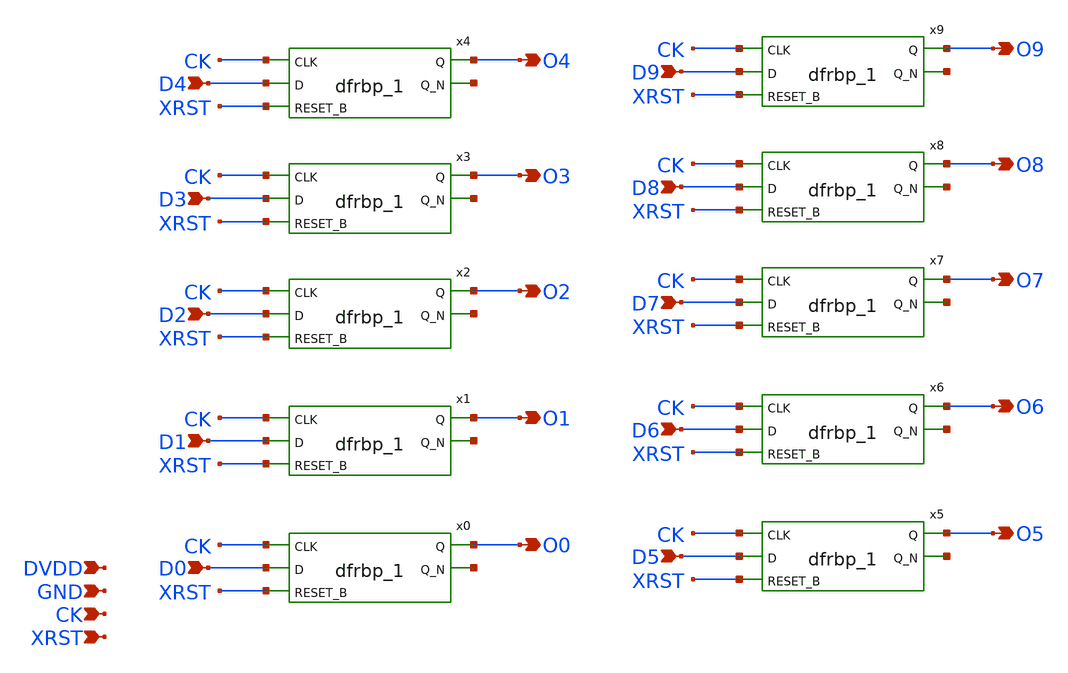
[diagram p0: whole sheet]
** sch_path: design/schematic/LATARRY_v1.sch
**.subckt LATARRY_v1 CK XRST DVDD GND D0 O0 D1 O1 D2 O2 D3 O3 D4 O4 D5 O5 D7 O7 D8 O6 D6 O8 D9 O9
*.ipin CK
*.ipin XRST
*.ipin DVDD
*.ipin GND
*.ipin D0
*.opin O0
*.ipin D1
*.opin O1
*.ipin D2
*.opin O2
*.ipin D3
*.opin O3
*.ipin D4
*.opin O4
*.ipin D5
*.opin O5
*.ipin D7
*.opin O7
*.ipin D8
*.opin O6
*.ipin D6
*.opin O8
*.ipin D9
*.opin O9
x0 CK D0 XRST GND GND DVDD DVDD O0 net1 sky130_fd_sc_hd__dfrbp_1
x1 CK D1 XRST GND GND DVDD DVDD O1 net2 sky130_fd_sc_hd__dfrbp_1
x2 CK D2 XRST GND GND DVDD DVDD O2 net3 sky130_fd_sc_hd__dfrbp_1
x3 CK D3 XRST GND GND DVDD DVDD O3 net4 sky130_fd_sc_hd__dfrbp_1
x4 CK D4 XRST GND GND DVDD DVDD O4 net5 sky130_fd_sc_hd__dfrbp_1
x5 CK D5 XRST GND GND DVDD DVDD O5 net6 sky130_fd_sc_hd__dfrbp_1
x6 CK D6 XRST GND GND DVDD DVDD O6 net7 sky130_fd_sc_hd__dfrbp_1
x7 CK D7 XRST GND GND DVDD DVDD O7 net8 sky130_fd_sc_hd__dfrbp_1
x8 CK D8 XRST GND GND DVDD DVDD O8 net9 sky130_fd_sc_hd__dfrbp_1
x9 CK D9 XRST GND GND DVDD DVDD O9 net10 sky130_fd_sc_hd__dfrbp_1
**.ends
.end
